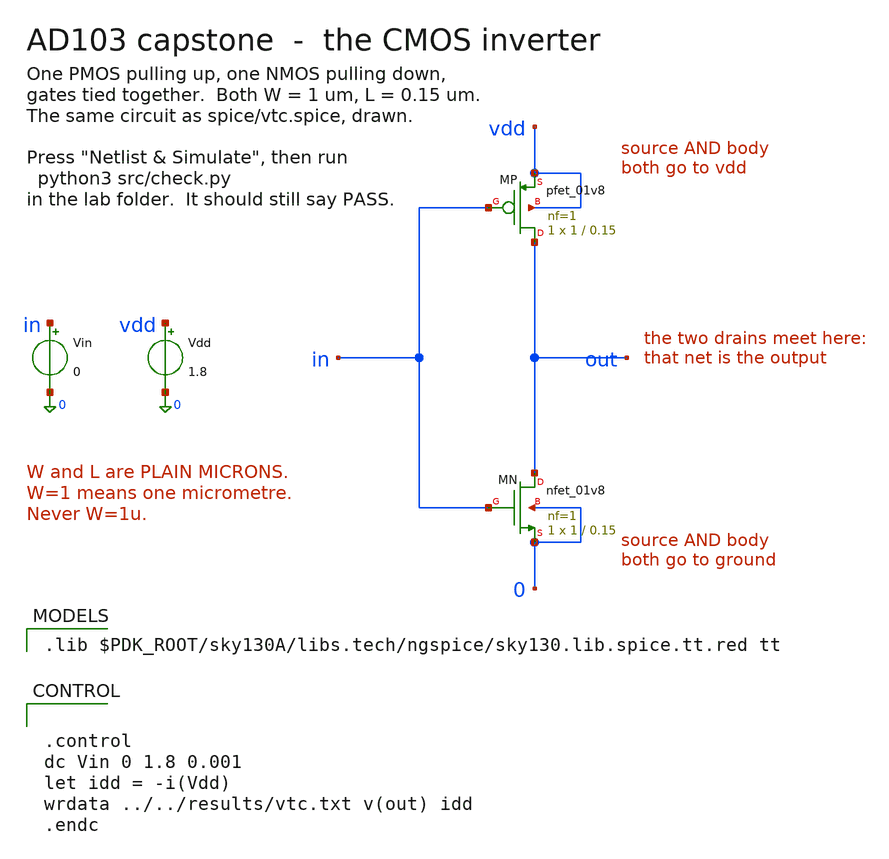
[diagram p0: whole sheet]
** sch_path: labs/capstone-inverter/xschem/inverter.sch
**.subckt inverter
XMP out in vdd vdd sky130_fd_pr__pfet_01v8 L=0.15 W=1 nf=1 ad='int((nf+1)/2) * W/nf * 0.29' as='int((nf+2)/2) * W/nf * 0.29'
+ pd='2*int((nf+1)/2) * (W/nf + 0.29)' ps='2*int((nf+2)/2) * (W/nf + 0.29)' nrd='0.29 / W' nrs='0.29 / W'
+ sa=0 sb=0 sd=0 mult=1 m=1
XMN out in 0 0 sky130_fd_pr__nfet_01v8 L=0.15 W=1 nf=1 ad='int((1 + 1)/2) * 1 / 1 * 0.29' as='int((1 + 2)/2) * 1 / 1 * 0.29'
+ pd='2*int((1 + 1)/2) * (1 / 1 + 0.29)' ps='2*int((1 + 2)/2) * (1 / 1 + 0.29)' nrd='0.29 / 1 ' nrs='0.29 / 1 '
+ sa=0 sb=0 sd=0 mult=1 m=1
Vdd vdd 0 1.8
Vin in 0 0
**** begin user architecture code

.lib $PDK_ROOT/sky130A/libs.tech/ngspice/sky130.lib.spice.tt.red tt



.control
dc Vin 0 1.8 0.001
let idd = -i(Vdd)
wrdata ../../results/vtc.txt v(out) idd
.endc


**** end user architecture code
**.ends
.end
